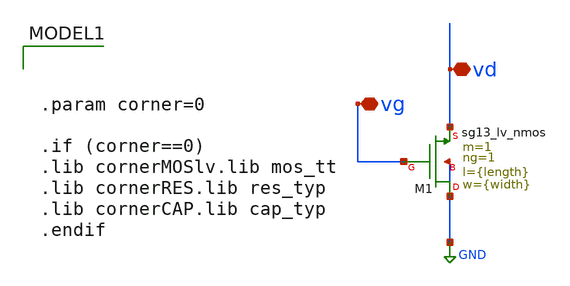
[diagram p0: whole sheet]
** sch_path: Tarea1/xschem/Length_sweep.sch
**.subckt Length_sweep vg vd
*.iopin vg
*.iopin vd
XM1 GND vg vd GND sg13_lv_nmos w={width} l={length} ng=1 m=1 mm_ok=1
**** begin user architecture code


.param corner=0

.if (corner==0)
.lib cornerMOSlv.lib mos_tt
.lib cornerRES.lib res_typ
.lib cornerCAP.lib cap_typ
.endif



.option wnflag=1
*vsup VDD 0 1.8
vin vg 0 dc=0.933 ac=1
vds vd 0 1.8
.param length = 0.13u
.param width = 4.38u
cload vd 0 5p
*.dc vin 0.0 1.8 0.01

.control
let strt_l = 2.33u
let stop_l = 3.23u
let step_l = 0.1u
let curr_l = strt_l

shell rm -f ao_sweep_l.raw

while curr_l le stop_l
    alterparam length = $&curr_l
    reset
    save all
    save @n.xm1.nsg13_lv_nmos[gm]
    save @n.xm1.nsg13_lv_nmos[gds]
    dc vds 0.02 1.8 0.01

    let gm = @n.xm1.nsg13_lv_nmos[gm]
    let gds = @n.xm1.nsg13_lv_nmos[gds]

    let ao = gm / gds
    *print ao

    set appendwrite
    wrdata ao_sweep_l.raw ao

    let curr_l = curr_l + step_l
end
.endc



**** end user architecture code
**.ends
.GLOBAL GND
.end
